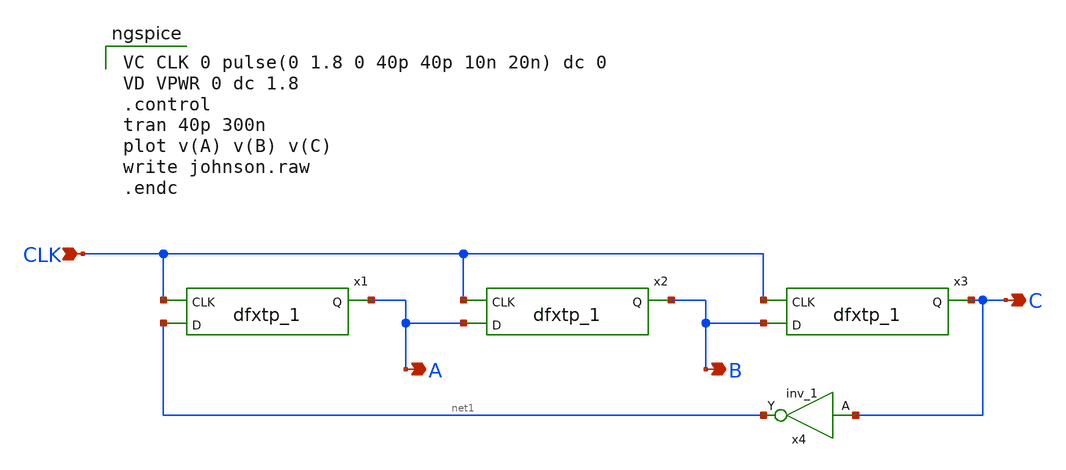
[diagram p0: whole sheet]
** sch_path: johnson.sch
**.subckt johnson A B C CLK
*.opin A
*.opin B
*.opin C
*.ipin CLK
x1 CLK net1 0 0 VPWR VPWR A sky130_fd_sc_hd__dfxtp_1
x2 CLK A 0 0 VPWR VPWR B sky130_fd_sc_hd__dfxtp_1
x3 CLK B 0 0 VPWR VPWR C sky130_fd_sc_hd__dfxtp_1
x4 C 0 0 VPWR VPWR net1 sky130_fd_sc_hd__inv_1
**** begin user architecture code

VC CLK 0 pulse(0 1.8 0 40p 40p 10n 20n) dc 0
VD VPWR 0 dc 1.8
.control
tran 40p 300n
plot v(A) v(B) v(C)
write johnson.raw
.endc


** opencircuitdesign pdks install
.lib $::SKYWATER_MODELS/sky130.lib.spice.tt.red tt
.include $::SKYWATER_STDCELLS/sky130_fd_sc_hd.spice

**** end user architecture code
**.ends
.end
